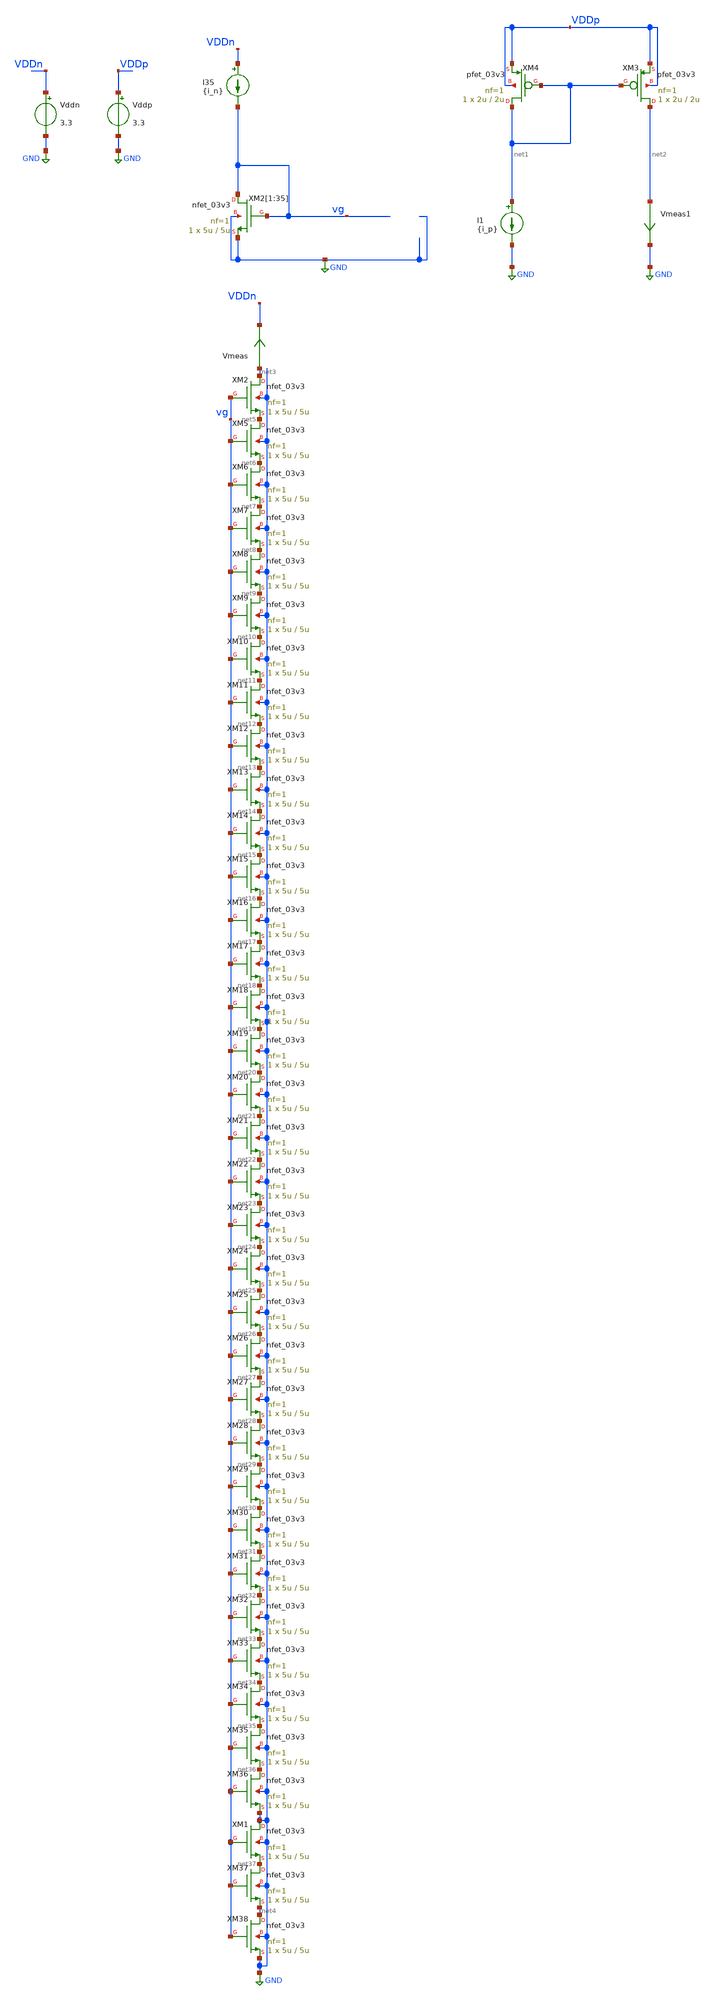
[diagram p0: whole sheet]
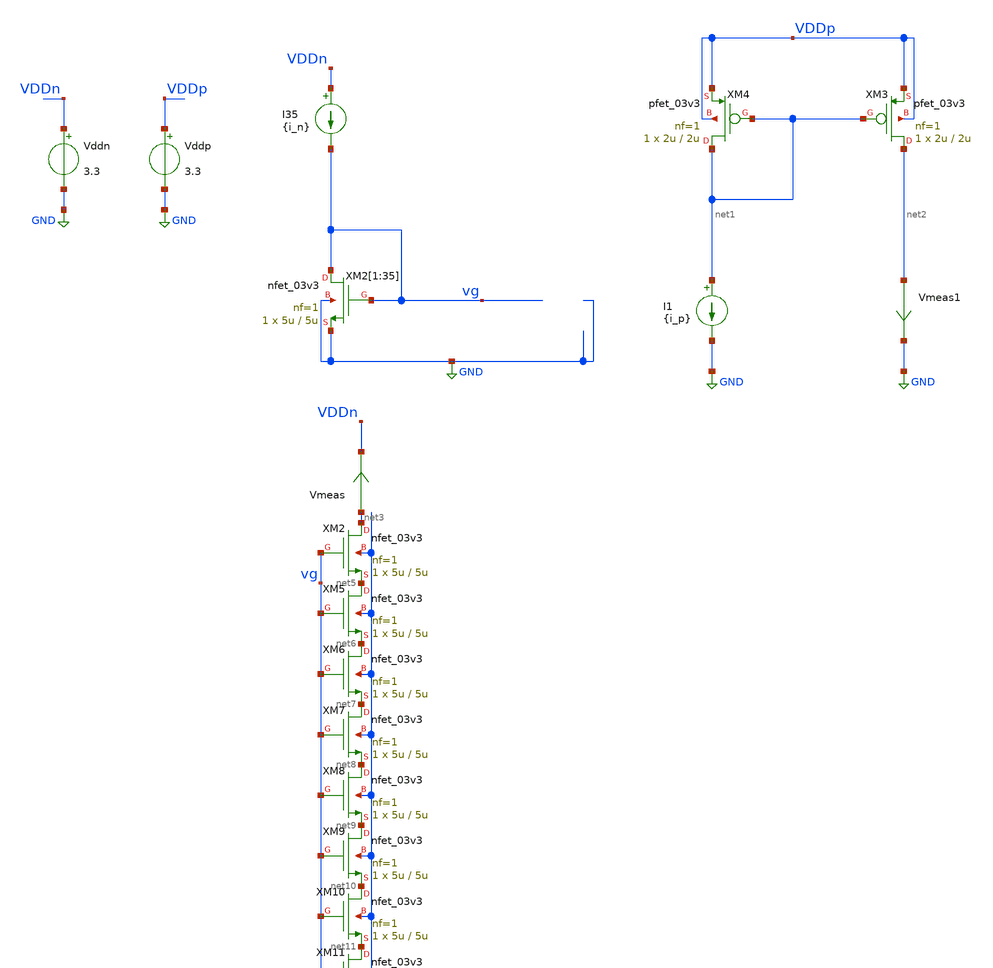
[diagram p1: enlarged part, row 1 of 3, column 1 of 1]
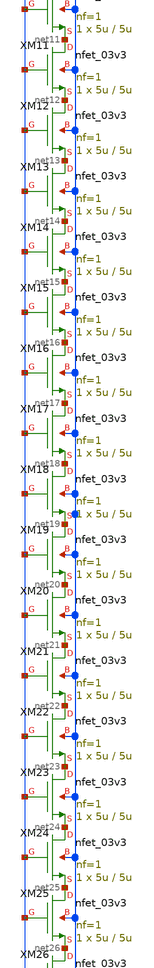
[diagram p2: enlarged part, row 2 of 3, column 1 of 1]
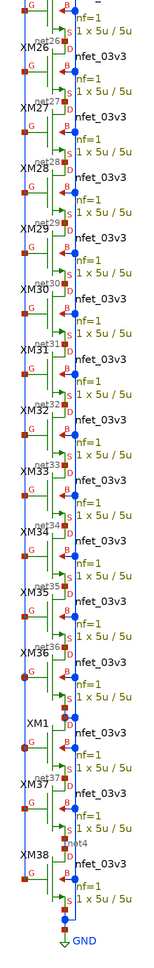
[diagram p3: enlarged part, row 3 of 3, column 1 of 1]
** sch_path: TIA_Filter/CurrentMirrors/TB_CM.sch
**.subckt TB_CM
XM2[1] vg vg GND GND nfet_03v3 L=5u W=5u nf=1 ad='int((nf+1)/2) * W/nf * 0.18u' as='int((nf+2)/2) * W/nf * 0.18u'
+ pd='2*int((nf+1)/2) * (W/nf + 0.18u)' ps='2*int((nf+2)/2) * (W/nf + 0.18u)' nrd='0.18u / W' nrs='0.18u / W'
+ sa=0 sb=0 sd=0 m=1
XM2[2] vg vg GND GND nfet_03v3 L=5u W=5u nf=1 ad='int((nf+1)/2) * W/nf * 0.18u' as='int((nf+2)/2) * W/nf * 0.18u'
+ pd='2*int((nf+1)/2) * (W/nf + 0.18u)' ps='2*int((nf+2)/2) * (W/nf + 0.18u)' nrd='0.18u / W' nrs='0.18u / W'
+ sa=0 sb=0 sd=0 m=1
XM2[3] vg vg GND GND nfet_03v3 L=5u W=5u nf=1 ad='int((nf+1)/2) * W/nf * 0.18u' as='int((nf+2)/2) * W/nf * 0.18u'
+ pd='2*int((nf+1)/2) * (W/nf + 0.18u)' ps='2*int((nf+2)/2) * (W/nf + 0.18u)' nrd='0.18u / W' nrs='0.18u / W'
+ sa=0 sb=0 sd=0 m=1
XM2[4] vg vg GND GND nfet_03v3 L=5u W=5u nf=1 ad='int((nf+1)/2) * W/nf * 0.18u' as='int((nf+2)/2) * W/nf * 0.18u'
+ pd='2*int((nf+1)/2) * (W/nf + 0.18u)' ps='2*int((nf+2)/2) * (W/nf + 0.18u)' nrd='0.18u / W' nrs='0.18u / W'
+ sa=0 sb=0 sd=0 m=1
XM2[5] vg vg GND GND nfet_03v3 L=5u W=5u nf=1 ad='int((nf+1)/2) * W/nf * 0.18u' as='int((nf+2)/2) * W/nf * 0.18u'
+ pd='2*int((nf+1)/2) * (W/nf + 0.18u)' ps='2*int((nf+2)/2) * (W/nf + 0.18u)' nrd='0.18u / W' nrs='0.18u / W'
+ sa=0 sb=0 sd=0 m=1
XM2[6] vg vg GND GND nfet_03v3 L=5u W=5u nf=1 ad='int((nf+1)/2) * W/nf * 0.18u' as='int((nf+2)/2) * W/nf * 0.18u'
+ pd='2*int((nf+1)/2) * (W/nf + 0.18u)' ps='2*int((nf+2)/2) * (W/nf + 0.18u)' nrd='0.18u / W' nrs='0.18u / W'
+ sa=0 sb=0 sd=0 m=1
XM2[7] vg vg GND GND nfet_03v3 L=5u W=5u nf=1 ad='int((nf+1)/2) * W/nf * 0.18u' as='int((nf+2)/2) * W/nf * 0.18u'
+ pd='2*int((nf+1)/2) * (W/nf + 0.18u)' ps='2*int((nf+2)/2) * (W/nf + 0.18u)' nrd='0.18u / W' nrs='0.18u / W'
+ sa=0 sb=0 sd=0 m=1
XM2[8] vg vg GND GND nfet_03v3 L=5u W=5u nf=1 ad='int((nf+1)/2) * W/nf * 0.18u' as='int((nf+2)/2) * W/nf * 0.18u'
+ pd='2*int((nf+1)/2) * (W/nf + 0.18u)' ps='2*int((nf+2)/2) * (W/nf + 0.18u)' nrd='0.18u / W' nrs='0.18u / W'
+ sa=0 sb=0 sd=0 m=1
XM2[9] vg vg GND GND nfet_03v3 L=5u W=5u nf=1 ad='int((nf+1)/2) * W/nf * 0.18u' as='int((nf+2)/2) * W/nf * 0.18u'
+ pd='2*int((nf+1)/2) * (W/nf + 0.18u)' ps='2*int((nf+2)/2) * (W/nf + 0.18u)' nrd='0.18u / W' nrs='0.18u / W'
+ sa=0 sb=0 sd=0 m=1
XM2[10] vg vg GND GND nfet_03v3 L=5u W=5u nf=1 ad='int((nf+1)/2) * W/nf * 0.18u' as='int((nf+2)/2) * W/nf * 0.18u'
+ pd='2*int((nf+1)/2) * (W/nf + 0.18u)' ps='2*int((nf+2)/2) * (W/nf + 0.18u)' nrd='0.18u / W' nrs='0.18u / W'
+ sa=0 sb=0 sd=0 m=1
XM2[11] vg vg GND GND nfet_03v3 L=5u W=5u nf=1 ad='int((nf+1)/2) * W/nf * 0.18u' as='int((nf+2)/2) * W/nf * 0.18u'
+ pd='2*int((nf+1)/2) * (W/nf + 0.18u)' ps='2*int((nf+2)/2) * (W/nf + 0.18u)' nrd='0.18u / W' nrs='0.18u / W'
+ sa=0 sb=0 sd=0 m=1
XM2[12] vg vg GND GND nfet_03v3 L=5u W=5u nf=1 ad='int((nf+1)/2) * W/nf * 0.18u' as='int((nf+2)/2) * W/nf * 0.18u'
+ pd='2*int((nf+1)/2) * (W/nf + 0.18u)' ps='2*int((nf+2)/2) * (W/nf + 0.18u)' nrd='0.18u / W' nrs='0.18u / W'
+ sa=0 sb=0 sd=0 m=1
XM2[13] vg vg GND GND nfet_03v3 L=5u W=5u nf=1 ad='int((nf+1)/2) * W/nf * 0.18u' as='int((nf+2)/2) * W/nf * 0.18u'
+ pd='2*int((nf+1)/2) * (W/nf + 0.18u)' ps='2*int((nf+2)/2) * (W/nf + 0.18u)' nrd='0.18u / W' nrs='0.18u / W'
+ sa=0 sb=0 sd=0 m=1
XM2[14] vg vg GND GND nfet_03v3 L=5u W=5u nf=1 ad='int((nf+1)/2) * W/nf * 0.18u' as='int((nf+2)/2) * W/nf * 0.18u'
+ pd='2*int((nf+1)/2) * (W/nf + 0.18u)' ps='2*int((nf+2)/2) * (W/nf + 0.18u)' nrd='0.18u / W' nrs='0.18u / W'
+ sa=0 sb=0 sd=0 m=1
XM2[15] vg vg GND GND nfet_03v3 L=5u W=5u nf=1 ad='int((nf+1)/2) * W/nf * 0.18u' as='int((nf+2)/2) * W/nf * 0.18u'
+ pd='2*int((nf+1)/2) * (W/nf + 0.18u)' ps='2*int((nf+2)/2) * (W/nf + 0.18u)' nrd='0.18u / W' nrs='0.18u / W'
+ sa=0 sb=0 sd=0 m=1
XM2[16] vg vg GND GND nfet_03v3 L=5u W=5u nf=1 ad='int((nf+1)/2) * W/nf * 0.18u' as='int((nf+2)/2) * W/nf * 0.18u'
+ pd='2*int((nf+1)/2) * (W/nf + 0.18u)' ps='2*int((nf+2)/2) * (W/nf + 0.18u)' nrd='0.18u / W' nrs='0.18u / W'
+ sa=0 sb=0 sd=0 m=1
XM2[17] vg vg GND GND nfet_03v3 L=5u W=5u nf=1 ad='int((nf+1)/2) * W/nf * 0.18u' as='int((nf+2)/2) * W/nf * 0.18u'
+ pd='2*int((nf+1)/2) * (W/nf + 0.18u)' ps='2*int((nf+2)/2) * (W/nf + 0.18u)' nrd='0.18u / W' nrs='0.18u / W'
+ sa=0 sb=0 sd=0 m=1
XM2[18] vg vg GND GND nfet_03v3 L=5u W=5u nf=1 ad='int((nf+1)/2) * W/nf * 0.18u' as='int((nf+2)/2) * W/nf * 0.18u'
+ pd='2*int((nf+1)/2) * (W/nf + 0.18u)' ps='2*int((nf+2)/2) * (W/nf + 0.18u)' nrd='0.18u / W' nrs='0.18u / W'
+ sa=0 sb=0 sd=0 m=1
XM2[19] vg vg GND GND nfet_03v3 L=5u W=5u nf=1 ad='int((nf+1)/2) * W/nf * 0.18u' as='int((nf+2)/2) * W/nf * 0.18u'
+ pd='2*int((nf+1)/2) * (W/nf + 0.18u)' ps='2*int((nf+2)/2) * (W/nf + 0.18u)' nrd='0.18u / W' nrs='0.18u / W'
+ sa=0 sb=0 sd=0 m=1
XM2[20] vg vg GND GND nfet_03v3 L=5u W=5u nf=1 ad='int((nf+1)/2) * W/nf * 0.18u' as='int((nf+2)/2) * W/nf * 0.18u'
+ pd='2*int((nf+1)/2) * (W/nf + 0.18u)' ps='2*int((nf+2)/2) * (W/nf + 0.18u)' nrd='0.18u / W' nrs='0.18u / W'
+ sa=0 sb=0 sd=0 m=1
XM2[21] vg vg GND GND nfet_03v3 L=5u W=5u nf=1 ad='int((nf+1)/2) * W/nf * 0.18u' as='int((nf+2)/2) * W/nf * 0.18u'
+ pd='2*int((nf+1)/2) * (W/nf + 0.18u)' ps='2*int((nf+2)/2) * (W/nf + 0.18u)' nrd='0.18u / W' nrs='0.18u / W'
+ sa=0 sb=0 sd=0 m=1
XM2[22] vg vg GND GND nfet_03v3 L=5u W=5u nf=1 ad='int((nf+1)/2) * W/nf * 0.18u' as='int((nf+2)/2) * W/nf * 0.18u'
+ pd='2*int((nf+1)/2) * (W/nf + 0.18u)' ps='2*int((nf+2)/2) * (W/nf + 0.18u)' nrd='0.18u / W' nrs='0.18u / W'
+ sa=0 sb=0 sd=0 m=1
XM2[23] vg vg GND GND nfet_03v3 L=5u W=5u nf=1 ad='int((nf+1)/2) * W/nf * 0.18u' as='int((nf+2)/2) * W/nf * 0.18u'
+ pd='2*int((nf+1)/2) * (W/nf + 0.18u)' ps='2*int((nf+2)/2) * (W/nf + 0.18u)' nrd='0.18u / W' nrs='0.18u / W'
+ sa=0 sb=0 sd=0 m=1
XM2[24] vg vg GND GND nfet_03v3 L=5u W=5u nf=1 ad='int((nf+1)/2) * W/nf * 0.18u' as='int((nf+2)/2) * W/nf * 0.18u'
+ pd='2*int((nf+1)/2) * (W/nf + 0.18u)' ps='2*int((nf+2)/2) * (W/nf + 0.18u)' nrd='0.18u / W' nrs='0.18u / W'
+ sa=0 sb=0 sd=0 m=1
XM2[25] vg vg GND GND nfet_03v3 L=5u W=5u nf=1 ad='int((nf+1)/2) * W/nf * 0.18u' as='int((nf+2)/2) * W/nf * 0.18u'
+ pd='2*int((nf+1)/2) * (W/nf + 0.18u)' ps='2*int((nf+2)/2) * (W/nf + 0.18u)' nrd='0.18u / W' nrs='0.18u / W'
+ sa=0 sb=0 sd=0 m=1
XM2[26] vg vg GND GND nfet_03v3 L=5u W=5u nf=1 ad='int((nf+1)/2) * W/nf * 0.18u' as='int((nf+2)/2) * W/nf * 0.18u'
+ pd='2*int((nf+1)/2) * (W/nf + 0.18u)' ps='2*int((nf+2)/2) * (W/nf + 0.18u)' nrd='0.18u / W' nrs='0.18u / W'
+ sa=0 sb=0 sd=0 m=1
XM2[27] vg vg GND GND nfet_03v3 L=5u W=5u nf=1 ad='int((nf+1)/2) * W/nf * 0.18u' as='int((nf+2)/2) * W/nf * 0.18u'
+ pd='2*int((nf+1)/2) * (W/nf + 0.18u)' ps='2*int((nf+2)/2) * (W/nf + 0.18u)' nrd='0.18u / W' nrs='0.18u / W'
+ sa=0 sb=0 sd=0 m=1
XM2[28] vg vg GND GND nfet_03v3 L=5u W=5u nf=1 ad='int((nf+1)/2) * W/nf * 0.18u' as='int((nf+2)/2) * W/nf * 0.18u'
+ pd='2*int((nf+1)/2) * (W/nf + 0.18u)' ps='2*int((nf+2)/2) * (W/nf + 0.18u)' nrd='0.18u / W' nrs='0.18u / W'
+ sa=0 sb=0 sd=0 m=1
XM2[29] vg vg GND GND nfet_03v3 L=5u W=5u nf=1 ad='int((nf+1)/2) * W/nf * 0.18u' as='int((nf+2)/2) * W/nf * 0.18u'
+ pd='2*int((nf+1)/2) * (W/nf + 0.18u)' ps='2*int((nf+2)/2) * (W/nf + 0.18u)' nrd='0.18u / W' nrs='0.18u / W'
+ sa=0 sb=0 sd=0 m=1
XM2[30] vg vg GND GND nfet_03v3 L=5u W=5u nf=1 ad='int((nf+1)/2) * W/nf * 0.18u' as='int((nf+2)/2) * W/nf * 0.18u'
+ pd='2*int((nf+1)/2) * (W/nf + 0.18u)' ps='2*int((nf+2)/2) * (W/nf + 0.18u)' nrd='0.18u / W' nrs='0.18u / W'
+ sa=0 sb=0 sd=0 m=1
XM2[31] vg vg GND GND nfet_03v3 L=5u W=5u nf=1 ad='int((nf+1)/2) * W/nf * 0.18u' as='int((nf+2)/2) * W/nf * 0.18u'
+ pd='2*int((nf+1)/2) * (W/nf + 0.18u)' ps='2*int((nf+2)/2) * (W/nf + 0.18u)' nrd='0.18u / W' nrs='0.18u / W'
+ sa=0 sb=0 sd=0 m=1
XM2[32] vg vg GND GND nfet_03v3 L=5u W=5u nf=1 ad='int((nf+1)/2) * W/nf * 0.18u' as='int((nf+2)/2) * W/nf * 0.18u'
+ pd='2*int((nf+1)/2) * (W/nf + 0.18u)' ps='2*int((nf+2)/2) * (W/nf + 0.18u)' nrd='0.18u / W' nrs='0.18u / W'
+ sa=0 sb=0 sd=0 m=1
XM2[33] vg vg GND GND nfet_03v3 L=5u W=5u nf=1 ad='int((nf+1)/2) * W/nf * 0.18u' as='int((nf+2)/2) * W/nf * 0.18u'
+ pd='2*int((nf+1)/2) * (W/nf + 0.18u)' ps='2*int((nf+2)/2) * (W/nf + 0.18u)' nrd='0.18u / W' nrs='0.18u / W'
+ sa=0 sb=0 sd=0 m=1
XM2[34] vg vg GND GND nfet_03v3 L=5u W=5u nf=1 ad='int((nf+1)/2) * W/nf * 0.18u' as='int((nf+2)/2) * W/nf * 0.18u'
+ pd='2*int((nf+1)/2) * (W/nf + 0.18u)' ps='2*int((nf+2)/2) * (W/nf + 0.18u)' nrd='0.18u / W' nrs='0.18u / W'
+ sa=0 sb=0 sd=0 m=1
XM2[35] vg vg GND GND nfet_03v3 L=5u W=5u nf=1 ad='int((nf+1)/2) * W/nf * 0.18u' as='int((nf+2)/2) * W/nf * 0.18u'
+ pd='2*int((nf+1)/2) * (W/nf + 0.18u)' ps='2*int((nf+2)/2) * (W/nf + 0.18u)' nrd='0.18u / W' nrs='0.18u / W'
+ sa=0 sb=0 sd=0 m=1
XM3 net2 net1 VDDp VDDp pfet_03v3 L=2u W=2u nf=1 ad='int((nf+1)/2) * W/nf * 0.18u' as='int((nf+2)/2) * W/nf * 0.18u'
+ pd='2*int((nf+1)/2) * (W/nf + 0.18u)' ps='2*int((nf+2)/2) * (W/nf + 0.18u)' nrd='0.18u / W' nrs='0.18u / W'
+ sa=0 sb=0 sd=0 m=1
XM4 net1 net1 VDDp VDDp pfet_03v3 L=2u W=2u nf=1 ad='int((nf+1)/2) * W/nf * 0.18u' as='int((nf+2)/2) * W/nf * 0.18u'
+ pd='2*int((nf+1)/2) * (W/nf + 0.18u)' ps='2*int((nf+2)/2) * (W/nf + 0.18u)' nrd='0.18u / W' nrs='0.18u / W'
+ sa=0 sb=0 sd=0 m=1
I35 VDDn vg {i_n}
I1 net1 GND {i_p}
Vddn VDDn GND 3.3
Vddp VDDp GND 3.3
Vmeas net3 VDDn 0
.save i(vmeas)
Vmeas1 net2 GND 0
.save i(vmeas1)
XM2 net3 vg net5 GND nfet_03v3 L=5u W=5u nf=1 ad='int((nf+1)/2) * W/nf * 0.18u' as='int((nf+2)/2) * W/nf * 0.18u'
+ pd='2*int((nf+1)/2) * (W/nf + 0.18u)' ps='2*int((nf+2)/2) * (W/nf + 0.18u)' nrd='0.18u / W' nrs='0.18u / W'
+ sa=0 sb=0 sd=0 m=1
XM5 net5 vg net6 GND nfet_03v3 L=5u W=5u nf=1 ad='int((nf+1)/2) * W/nf * 0.18u' as='int((nf+2)/2) * W/nf * 0.18u'
+ pd='2*int((nf+1)/2) * (W/nf + 0.18u)' ps='2*int((nf+2)/2) * (W/nf + 0.18u)' nrd='0.18u / W' nrs='0.18u / W'
+ sa=0 sb=0 sd=0 m=1
XM6 net6 vg net7 GND nfet_03v3 L=5u W=5u nf=1 ad='int((nf+1)/2) * W/nf * 0.18u' as='int((nf+2)/2) * W/nf * 0.18u'
+ pd='2*int((nf+1)/2) * (W/nf + 0.18u)' ps='2*int((nf+2)/2) * (W/nf + 0.18u)' nrd='0.18u / W' nrs='0.18u / W'
+ sa=0 sb=0 sd=0 m=1
XM7 net7 vg net8 GND nfet_03v3 L=5u W=5u nf=1 ad='int((nf+1)/2) * W/nf * 0.18u' as='int((nf+2)/2) * W/nf * 0.18u'
+ pd='2*int((nf+1)/2) * (W/nf + 0.18u)' ps='2*int((nf+2)/2) * (W/nf + 0.18u)' nrd='0.18u / W' nrs='0.18u / W'
+ sa=0 sb=0 sd=0 m=1
XM8 net8 vg net9 GND nfet_03v3 L=5u W=5u nf=1 ad='int((nf+1)/2) * W/nf * 0.18u' as='int((nf+2)/2) * W/nf * 0.18u'
+ pd='2*int((nf+1)/2) * (W/nf + 0.18u)' ps='2*int((nf+2)/2) * (W/nf + 0.18u)' nrd='0.18u / W' nrs='0.18u / W'
+ sa=0 sb=0 sd=0 m=1
XM9 net9 vg net10 GND nfet_03v3 L=5u W=5u nf=1 ad='int((nf+1)/2) * W/nf * 0.18u' as='int((nf+2)/2) * W/nf * 0.18u'
+ pd='2*int((nf+1)/2) * (W/nf + 0.18u)' ps='2*int((nf+2)/2) * (W/nf + 0.18u)' nrd='0.18u / W' nrs='0.18u / W'
+ sa=0 sb=0 sd=0 m=1
XM10 net10 vg net11 GND nfet_03v3 L=5u W=5u nf=1 ad='int((nf+1)/2) * W/nf * 0.18u' as='int((nf+2)/2) * W/nf * 0.18u'
+ pd='2*int((nf+1)/2) * (W/nf + 0.18u)' ps='2*int((nf+2)/2) * (W/nf + 0.18u)' nrd='0.18u / W' nrs='0.18u / W'
+ sa=0 sb=0 sd=0 m=1
XM11 net11 vg net12 GND nfet_03v3 L=5u W=5u nf=1 ad='int((nf+1)/2) * W/nf * 0.18u' as='int((nf+2)/2) * W/nf * 0.18u'
+ pd='2*int((nf+1)/2) * (W/nf + 0.18u)' ps='2*int((nf+2)/2) * (W/nf + 0.18u)' nrd='0.18u / W' nrs='0.18u / W'
+ sa=0 sb=0 sd=0 m=1
XM12 net12 vg net13 GND nfet_03v3 L=5u W=5u nf=1 ad='int((nf+1)/2) * W/nf * 0.18u' as='int((nf+2)/2) * W/nf * 0.18u'
+ pd='2*int((nf+1)/2) * (W/nf + 0.18u)' ps='2*int((nf+2)/2) * (W/nf + 0.18u)' nrd='0.18u / W' nrs='0.18u / W'
+ sa=0 sb=0 sd=0 m=1
XM13 net13 vg net14 GND nfet_03v3 L=5u W=5u nf=1 ad='int((nf+1)/2) * W/nf * 0.18u' as='int((nf+2)/2) * W/nf * 0.18u'
+ pd='2*int((nf+1)/2) * (W/nf + 0.18u)' ps='2*int((nf+2)/2) * (W/nf + 0.18u)' nrd='0.18u / W' nrs='0.18u / W'
+ sa=0 sb=0 sd=0 m=1
XM14 net14 vg net15 GND nfet_03v3 L=5u W=5u nf=1 ad='int((nf+1)/2) * W/nf * 0.18u' as='int((nf+2)/2) * W/nf * 0.18u'
+ pd='2*int((nf+1)/2) * (W/nf + 0.18u)' ps='2*int((nf+2)/2) * (W/nf + 0.18u)' nrd='0.18u / W' nrs='0.18u / W'
+ sa=0 sb=0 sd=0 m=1
XM15 net15 vg net16 GND nfet_03v3 L=5u W=5u nf=1 ad='int((nf+1)/2) * W/nf * 0.18u' as='int((nf+2)/2) * W/nf * 0.18u'
+ pd='2*int((nf+1)/2) * (W/nf + 0.18u)' ps='2*int((nf+2)/2) * (W/nf + 0.18u)' nrd='0.18u / W' nrs='0.18u / W'
+ sa=0 sb=0 sd=0 m=1
XM16 net16 vg net17 GND nfet_03v3 L=5u W=5u nf=1 ad='int((nf+1)/2) * W/nf * 0.18u' as='int((nf+2)/2) * W/nf * 0.18u'
+ pd='2*int((nf+1)/2) * (W/nf + 0.18u)' ps='2*int((nf+2)/2) * (W/nf + 0.18u)' nrd='0.18u / W' nrs='0.18u / W'
+ sa=0 sb=0 sd=0 m=1
XM17 net17 vg net18 GND nfet_03v3 L=5u W=5u nf=1 ad='int((nf+1)/2) * W/nf * 0.18u' as='int((nf+2)/2) * W/nf * 0.18u'
+ pd='2*int((nf+1)/2) * (W/nf + 0.18u)' ps='2*int((nf+2)/2) * (W/nf + 0.18u)' nrd='0.18u / W' nrs='0.18u / W'
+ sa=0 sb=0 sd=0 m=1
XM18 net18 vg net19 GND nfet_03v3 L=5u W=5u nf=1 ad='int((nf+1)/2) * W/nf * 0.18u' as='int((nf+2)/2) * W/nf * 0.18u'
+ pd='2*int((nf+1)/2) * (W/nf + 0.18u)' ps='2*int((nf+2)/2) * (W/nf + 0.18u)' nrd='0.18u / W' nrs='0.18u / W'
+ sa=0 sb=0 sd=0 m=1
XM19 net19 vg net20 GND nfet_03v3 L=5u W=5u nf=1 ad='int((nf+1)/2) * W/nf * 0.18u' as='int((nf+2)/2) * W/nf * 0.18u'
+ pd='2*int((nf+1)/2) * (W/nf + 0.18u)' ps='2*int((nf+2)/2) * (W/nf + 0.18u)' nrd='0.18u / W' nrs='0.18u / W'
+ sa=0 sb=0 sd=0 m=1
XM20 net20 vg net21 GND nfet_03v3 L=5u W=5u nf=1 ad='int((nf+1)/2) * W/nf * 0.18u' as='int((nf+2)/2) * W/nf * 0.18u'
+ pd='2*int((nf+1)/2) * (W/nf + 0.18u)' ps='2*int((nf+2)/2) * (W/nf + 0.18u)' nrd='0.18u / W' nrs='0.18u / W'
+ sa=0 sb=0 sd=0 m=1
XM21 net21 vg net22 GND nfet_03v3 L=5u W=5u nf=1 ad='int((nf+1)/2) * W/nf * 0.18u' as='int((nf+2)/2) * W/nf * 0.18u'
+ pd='2*int((nf+1)/2) * (W/nf + 0.18u)' ps='2*int((nf+2)/2) * (W/nf + 0.18u)' nrd='0.18u / W' nrs='0.18u / W'
+ sa=0 sb=0 sd=0 m=1
XM22 net22 vg net23 GND nfet_03v3 L=5u W=5u nf=1 ad='int((nf+1)/2) * W/nf * 0.18u' as='int((nf+2)/2) * W/nf * 0.18u'
+ pd='2*int((nf+1)/2) * (W/nf + 0.18u)' ps='2*int((nf+2)/2) * (W/nf + 0.18u)' nrd='0.18u / W' nrs='0.18u / W'
+ sa=0 sb=0 sd=0 m=1
XM23 net23 vg net24 GND nfet_03v3 L=5u W=5u nf=1 ad='int((nf+1)/2) * W/nf * 0.18u' as='int((nf+2)/2) * W/nf * 0.18u'
+ pd='2*int((nf+1)/2) * (W/nf + 0.18u)' ps='2*int((nf+2)/2) * (W/nf + 0.18u)' nrd='0.18u / W' nrs='0.18u / W'
+ sa=0 sb=0 sd=0 m=1
XM24 net24 vg net25 GND nfet_03v3 L=5u W=5u nf=1 ad='int((nf+1)/2) * W/nf * 0.18u' as='int((nf+2)/2) * W/nf * 0.18u'
+ pd='2*int((nf+1)/2) * (W/nf + 0.18u)' ps='2*int((nf+2)/2) * (W/nf + 0.18u)' nrd='0.18u / W' nrs='0.18u / W'
+ sa=0 sb=0 sd=0 m=1
XM25 net25 vg net26 GND nfet_03v3 L=5u W=5u nf=1 ad='int((nf+1)/2) * W/nf * 0.18u' as='int((nf+2)/2) * W/nf * 0.18u'
+ pd='2*int((nf+1)/2) * (W/nf + 0.18u)' ps='2*int((nf+2)/2) * (W/nf + 0.18u)' nrd='0.18u / W' nrs='0.18u / W'
+ sa=0 sb=0 sd=0 m=1
XM26 net26 vg net27 GND nfet_03v3 L=5u W=5u nf=1 ad='int((nf+1)/2) * W/nf * 0.18u' as='int((nf+2)/2) * W/nf * 0.18u'
+ pd='2*int((nf+1)/2) * (W/nf + 0.18u)' ps='2*int((nf+2)/2) * (W/nf + 0.18u)' nrd='0.18u / W' nrs='0.18u / W'
+ sa=0 sb=0 sd=0 m=1
XM27 net27 vg net28 GND nfet_03v3 L=5u W=5u nf=1 ad='int((nf+1)/2) * W/nf * 0.18u' as='int((nf+2)/2) * W/nf * 0.18u'
+ pd='2*int((nf+1)/2) * (W/nf + 0.18u)' ps='2*int((nf+2)/2) * (W/nf + 0.18u)' nrd='0.18u / W' nrs='0.18u / W'
+ sa=0 sb=0 sd=0 m=1
XM28 net28 vg net29 GND nfet_03v3 L=5u W=5u nf=1 ad='int((nf+1)/2) * W/nf * 0.18u' as='int((nf+2)/2) * W/nf * 0.18u'
+ pd='2*int((nf+1)/2) * (W/nf + 0.18u)' ps='2*int((nf+2)/2) * (W/nf + 0.18u)' nrd='0.18u / W' nrs='0.18u / W'
+ sa=0 sb=0 sd=0 m=1
XM29 net29 vg net30 GND nfet_03v3 L=5u W=5u nf=1 ad='int((nf+1)/2) * W/nf * 0.18u' as='int((nf+2)/2) * W/nf * 0.18u'
+ pd='2*int((nf+1)/2) * (W/nf + 0.18u)' ps='2*int((nf+2)/2) * (W/nf + 0.18u)' nrd='0.18u / W' nrs='0.18u / W'
+ sa=0 sb=0 sd=0 m=1
XM30 net30 vg net31 GND nfet_03v3 L=5u W=5u nf=1 ad='int((nf+1)/2) * W/nf * 0.18u' as='int((nf+2)/2) * W/nf * 0.18u'
+ pd='2*int((nf+1)/2) * (W/nf + 0.18u)' ps='2*int((nf+2)/2) * (W/nf + 0.18u)' nrd='0.18u / W' nrs='0.18u / W'
+ sa=0 sb=0 sd=0 m=1
XM31 net31 vg net32 GND nfet_03v3 L=5u W=5u nf=1 ad='int((nf+1)/2) * W/nf * 0.18u' as='int((nf+2)/2) * W/nf * 0.18u'
+ pd='2*int((nf+1)/2) * (W/nf + 0.18u)' ps='2*int((nf+2)/2) * (W/nf + 0.18u)' nrd='0.18u / W' nrs='0.18u / W'
+ sa=0 sb=0 sd=0 m=1
XM32 net32 vg net33 GND nfet_03v3 L=5u W=5u nf=1 ad='int((nf+1)/2) * W/nf * 0.18u' as='int((nf+2)/2) * W/nf * 0.18u'
+ pd='2*int((nf+1)/2) * (W/nf + 0.18u)' ps='2*int((nf+2)/2) * (W/nf + 0.18u)' nrd='0.18u / W' nrs='0.18u / W'
+ sa=0 sb=0 sd=0 m=1
XM33 net33 vg net34 GND nfet_03v3 L=5u W=5u nf=1 ad='int((nf+1)/2) * W/nf * 0.18u' as='int((nf+2)/2) * W/nf * 0.18u'
+ pd='2*int((nf+1)/2) * (W/nf + 0.18u)' ps='2*int((nf+2)/2) * (W/nf + 0.18u)' nrd='0.18u / W' nrs='0.18u / W'
+ sa=0 sb=0 sd=0 m=1
XM34 net34 vg net35 GND nfet_03v3 L=5u W=5u nf=1 ad='int((nf+1)/2) * W/nf * 0.18u' as='int((nf+2)/2) * W/nf * 0.18u'
+ pd='2*int((nf+1)/2) * (W/nf + 0.18u)' ps='2*int((nf+2)/2) * (W/nf + 0.18u)' nrd='0.18u / W' nrs='0.18u / W'
+ sa=0 sb=0 sd=0 m=1
XM35 net35 vg net36 GND nfet_03v3 L=5u W=5u nf=1 ad='int((nf+1)/2) * W/nf * 0.18u' as='int((nf+2)/2) * W/nf * 0.18u'
+ pd='2*int((nf+1)/2) * (W/nf + 0.18u)' ps='2*int((nf+2)/2) * (W/nf + 0.18u)' nrd='0.18u / W' nrs='0.18u / W'
+ sa=0 sb=0 sd=0 m=1
XM36 net36 vg GND GND nfet_03v3 L=5u W=5u nf=1 ad='int((nf+1)/2) * W/nf * 0.18u' as='int((nf+2)/2) * W/nf * 0.18u'
+ pd='2*int((nf+1)/2) * (W/nf + 0.18u)' ps='2*int((nf+2)/2) * (W/nf + 0.18u)' nrd='0.18u / W' nrs='0.18u / W'
+ sa=0 sb=0 sd=0 m=1
XM1 GND vg net37 GND nfet_03v3 L=5u W=5u nf=1 ad='int((nf+1)/2) * W/nf * 0.18u' as='int((nf+2)/2) * W/nf * 0.18u'
+ pd='2*int((nf+1)/2) * (W/nf + 0.18u)' ps='2*int((nf+2)/2) * (W/nf + 0.18u)' nrd='0.18u / W' nrs='0.18u / W'
+ sa=0 sb=0 sd=0 m=1
XM37 net37 vg net4 GND nfet_03v3 L=5u W=5u nf=1 ad='int((nf+1)/2) * W/nf * 0.18u' as='int((nf+2)/2) * W/nf * 0.18u'
+ pd='2*int((nf+1)/2) * (W/nf + 0.18u)' ps='2*int((nf+2)/2) * (W/nf + 0.18u)' nrd='0.18u / W' nrs='0.18u / W'
+ sa=0 sb=0 sd=0 m=1
XM38 net4 vg GND GND nfet_03v3 L=5u W=5u nf=1 ad='int((nf+1)/2) * W/nf * 0.18u' as='int((nf+2)/2) * W/nf * 0.18u'
+ pd='2*int((nf+1)/2) * (W/nf + 0.18u)' ps='2*int((nf+2)/2) * (W/nf + 0.18u)' nrd='0.18u / W' nrs='0.18u / W'
+ sa=0 sb=0 sd=0 m=1
**** begin user architecture code

.include $::180MCU_MODELS/design.ngspice
.lib $::180MCU_MODELS/sm141064.ngspice typical
.param sw_stat_mismatch=1
.param sw_stat_global=1



.option gmin=1e-18
.param i_n=1n
.param i_p=1n

.control
save all

let sample_num = 0

while sample_num<151

reset
op
remzerovec
write TB_CM.raw
wrdata /home/lci-ufsc/Desktop/Bracolin/TIA_Filter/CurrentMirrors/out_cm.txt i(Vmeas)
set appendwrite

let sample_num = sample_num + 1
end


.endc
.save all


**** end user architecture code
**.ends
.GLOBAL GND
.end
